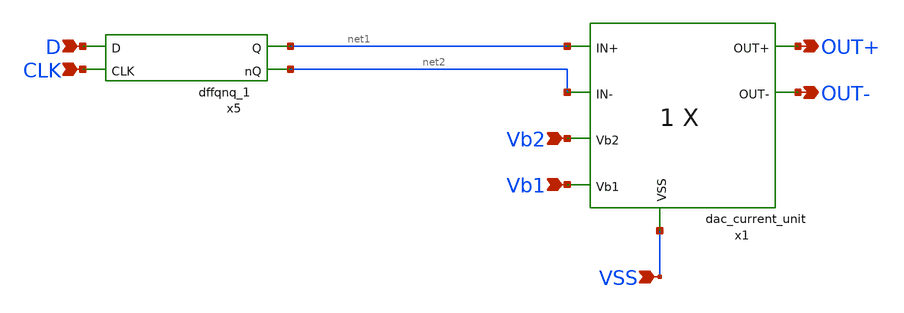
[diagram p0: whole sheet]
** sch_path: DAC/xschem/dac_current_cell_1X.sch
**.subckt dac_current_cell_1X VSS OUT+ OUT- Vb2 Vb1 D CLK
*.ipin VSS
*.opin OUT+
*.opin OUT-
*.ipin Vb2
*.ipin Vb1
*.ipin D
*.ipin CLK
x1 OUT+ OUT- net1 net2 Vb2 Vb1 VSS dac_current_unit nf=1
x5 D net1 CLK net2 DVDD DVNW DVPW DVSS dffqnq_1
**.ends

* expanding   symbol:  dac_current_unit.sym # of pins=7
** sym_path: DAC/xschem/dac_current_unit.sym
** sch_path: DAC/xschem/dac_current_unit.sch
.subckt dac_current_unit OUT+ OUT- IN+ IN- Vb2 Vb1 VSS  nf=1
*.ipin IN+
*.ipin IN-
*.opin OUT-
*.opin OUT+
*.ipin Vb2
*.ipin Vb1
*.ipin VSS
XM1 net1 Vb2 net2 VSS nfet_03v3 L=0.5u W=nf*2u nf=nf ad='int((nf+1)/2) * W/nf * 0.18u' as='int((nf+2)/2) * W/nf * 0.18u'
+ pd='2*int((nf+1)/2) * (W/nf + 0.18u)' ps='2*int((nf+2)/2) * (W/nf + 0.18u)' nrd='0.18u / W' nrs='0.18u / W'
+ sa=0 sb=0 sd=0 m=1
XM2 net2 Vb1 VSS VSS nfet_03v3 L=1u W=nf*2u nf=nf ad='int((nf+1)/2) * W/nf * 0.18u' as='int((nf+2)/2) * W/nf * 0.18u'
+ pd='2*int((nf+1)/2) * (W/nf + 0.18u)' ps='2*int((nf+2)/2) * (W/nf + 0.18u)' nrd='0.18u / W' nrs='0.18u / W'
+ sa=0 sb=0 sd=0 m=1
XM5 OUT+ IN+ net1 VSS nfet_03v3 L=0.28u W=nf*1u nf=nf ad='int((nf+1)/2) * W/nf * 0.18u' as='int((nf+2)/2) * W/nf * 0.18u'
+ pd='2*int((nf+1)/2) * (W/nf + 0.18u)' ps='2*int((nf+2)/2) * (W/nf + 0.18u)' nrd='0.18u / W' nrs='0.18u / W'
+ sa=0 sb=0 sd=0 m=1
XM6 OUT- IN- net1 VSS nfet_03v3 L=0.28u W=nf*1u nf=nf ad='int((nf+1)/2) * W/nf * 0.18u' as='int((nf+2)/2) * W/nf * 0.18u'
+ pd='2*int((nf+1)/2) * (W/nf + 0.18u)' ps='2*int((nf+2)/2) * (W/nf + 0.18u)' nrd='0.18u / W' nrs='0.18u / W'
+ sa=0 sb=0 sd=0 m=1
.ends


* expanding   symbol:  std_cell/dffqnq_1.sym # of pins=4
** sym_path: DAC/xschem/std_cell/dffqnq_1.sym
** sch_path: DAC/xschem/std_cell/dffqnq_1.sch
.subckt dffqnq_1 D Q CLK nQ VDD VNW VPW VSS
*.ipin D
*.ipin CLK
*.opin Q
*.opin nQ
x1 D CLK Q VDD VNW VPW VSS gf180mcu_fd_sc_mcu7t5v0__dffq_1
x2 Q nQ VDD VNW VPW VSS gf180mcu_fd_sc_mcu7t5v0__inv_1
.ends

.end
